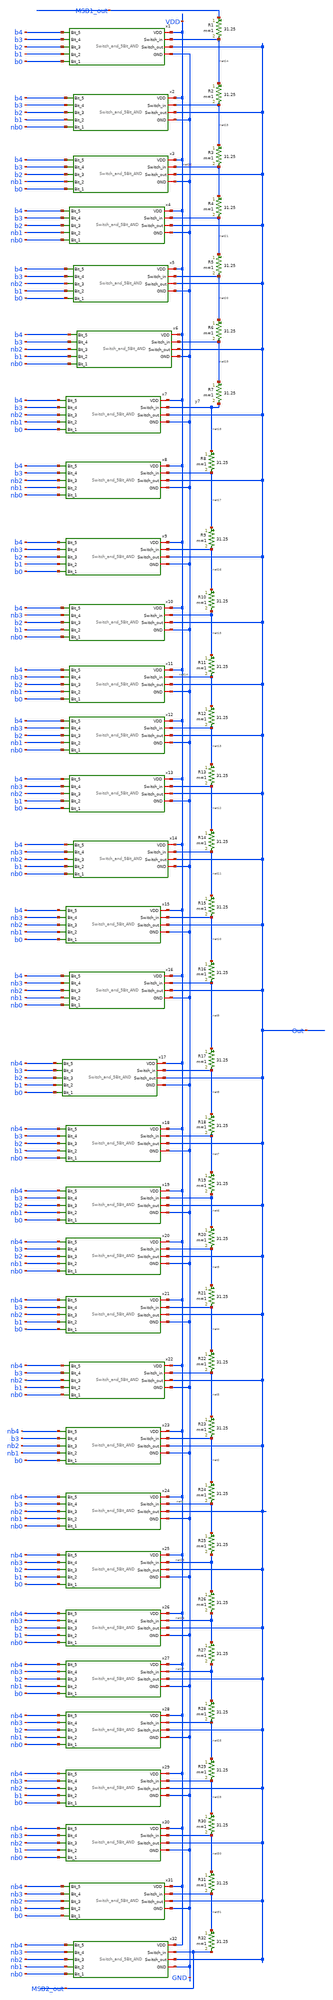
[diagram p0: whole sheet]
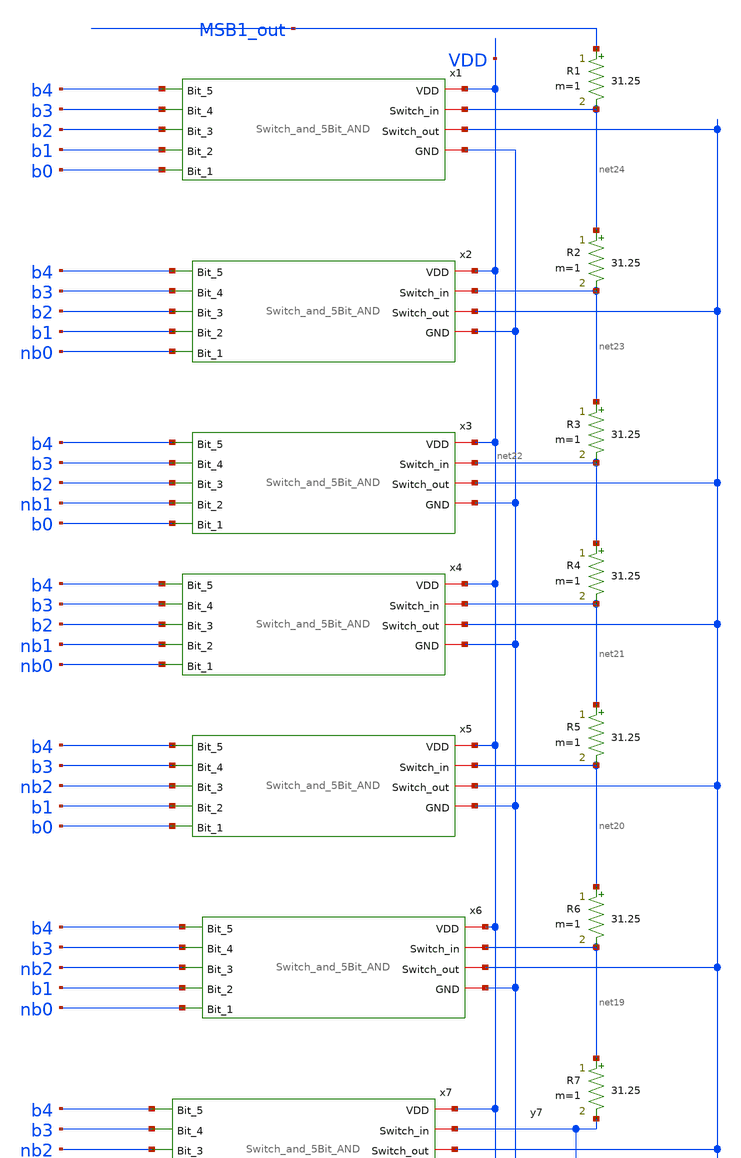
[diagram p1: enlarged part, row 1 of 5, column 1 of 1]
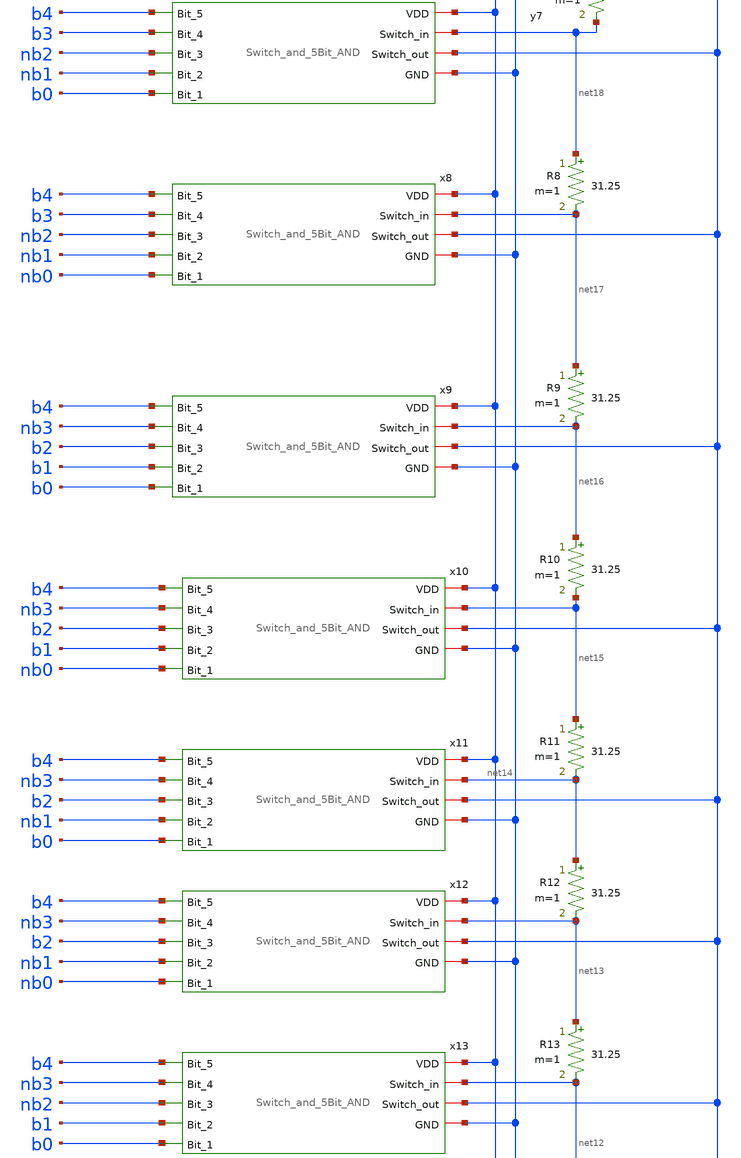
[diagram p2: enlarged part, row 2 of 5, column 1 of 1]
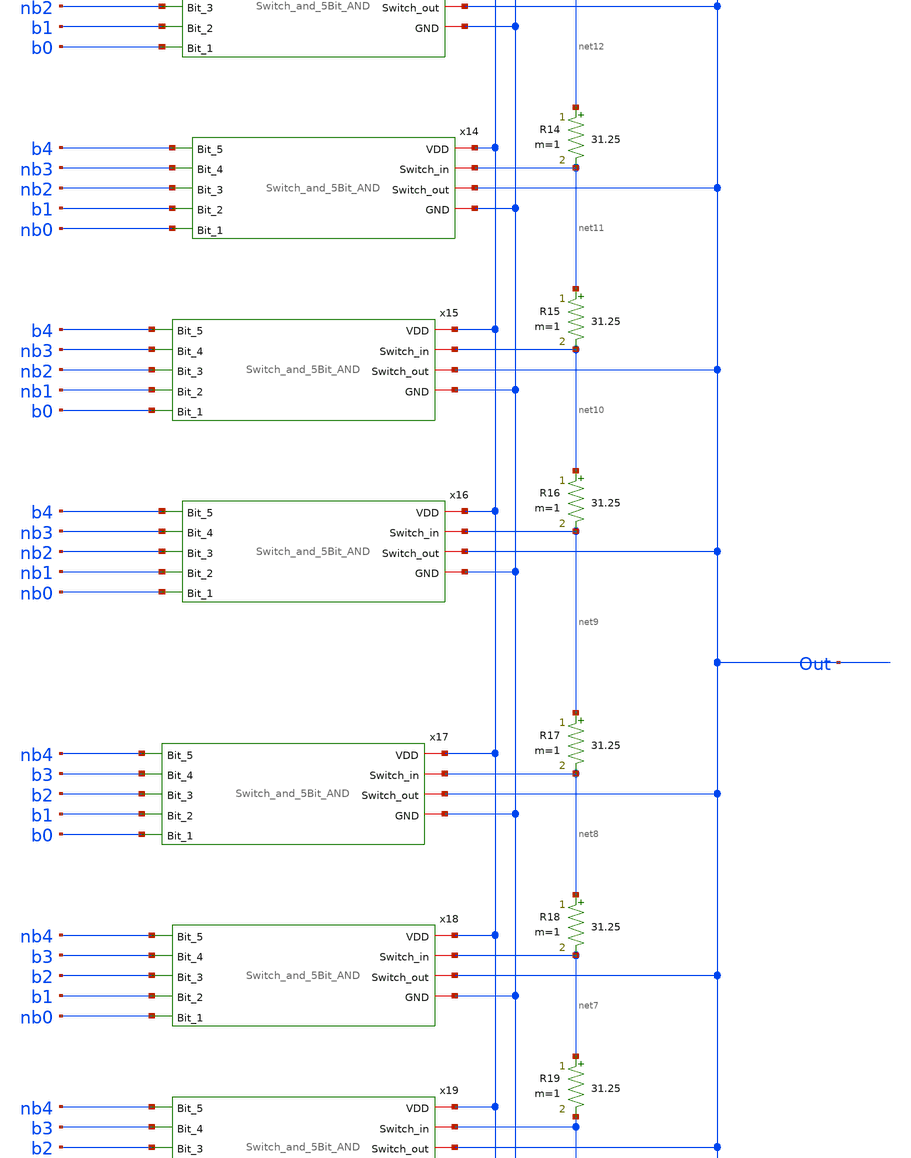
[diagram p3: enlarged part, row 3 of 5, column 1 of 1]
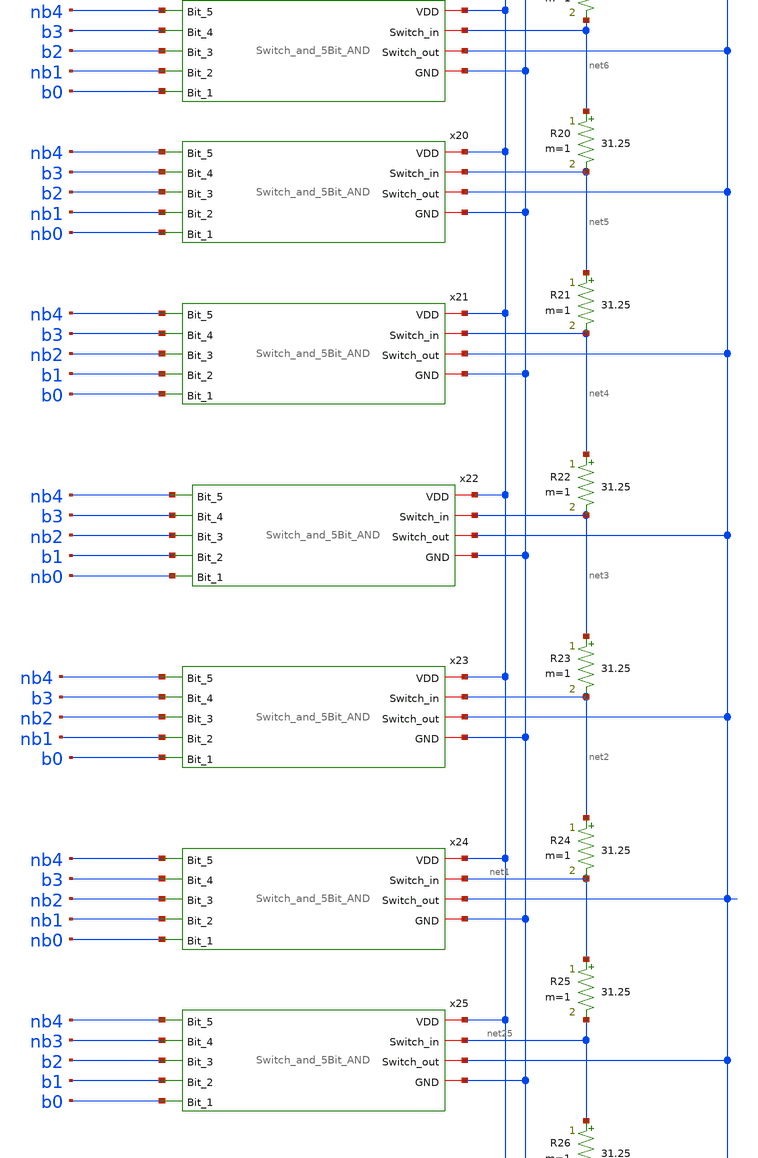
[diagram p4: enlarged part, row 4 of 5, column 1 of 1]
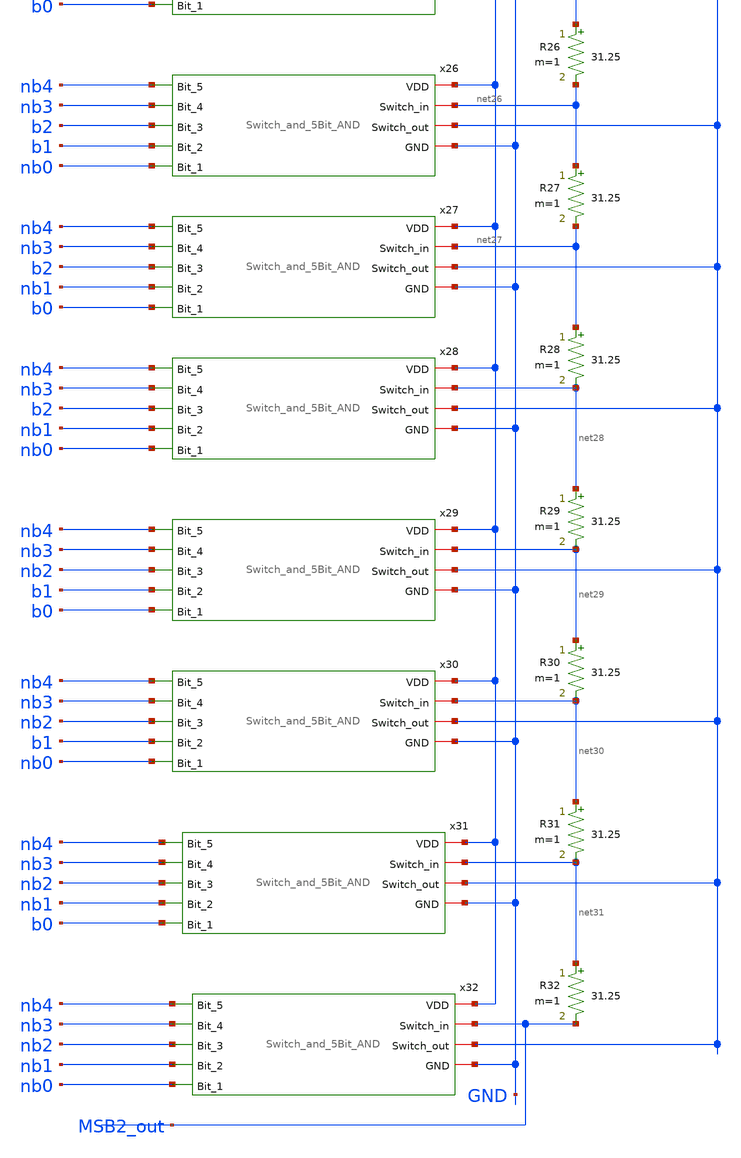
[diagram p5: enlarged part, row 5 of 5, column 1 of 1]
** sch_path: ProjectDesigns/10bitDAC/lsb.sch
**.subckt lsb
R1 MSB1_out net24 31.25 m=1
R2 net24 net23 31.25 m=1
R3 net23 net22 31.25 m=1
R4 net22 net21 31.25 m=1
R5 net21 net20 31.25 m=1
R6 net20 net19 31.25 m=1
R7 net19 net18 31.25 m=1
R8 net18 net17 31.25 m=1
R9 net17 net16 31.25 m=1
R10 net16 net15 31.25 m=1
R11 net15 net14 31.25 m=1
R12 net14 net13 31.25 m=1
R13 net13 net12 31.25 m=1
R14 net12 net11 31.25 m=1
R15 net11 net10 31.25 m=1
R16 net10 net9 31.25 m=1
R17 net9 net8 31.25 m=1
R18 net8 net7 31.25 m=1
R19 net7 net6 31.25 m=1
R20 net6 net5 31.25 m=1
R21 net5 net4 31.25 m=1
R22 net4 net3 31.25 m=1
R23 net3 net2 31.25 m=1
R24 net2 net1 31.25 m=1
R25 net1 net25 31.25 m=1
R26 net25 net26 31.25 m=1
R27 net26 net27 31.25 m=1
R28 net27 net28 31.25 m=1
R29 net28 net29 31.25 m=1
R30 net29 net30 31.25 m=1
R31 net30 net31 31.25 m=1
R32 net31 MSB2_out 31.25 m=1
x1 VDD b4 b3 net24 b2 Out b1 GND b0 Switch_and_5Bit_AND
x2 VDD b4 b3 net23 b2 Out b1 GND nb0 Switch_and_5Bit_AND
x3 VDD b4 b3 net22 b2 Out nb1 GND b0 Switch_and_5Bit_AND
x4 VDD b4 b3 net21 b2 Out nb1 GND nb0 Switch_and_5Bit_AND
x5 VDD b4 b3 net20 nb2 Out b1 GND b0 Switch_and_5Bit_AND
x6 VDD b4 b3 net19 nb2 Out b1 GND nb0 Switch_and_5Bit_AND
x7 VDD b4 b3 net18 nb2 Out nb1 GND b0 Switch_and_5Bit_AND
x8 VDD b4 b3 net17 nb2 Out nb1 GND nb0 Switch_and_5Bit_AND
x9 VDD b4 nb3 net16 b2 Out b1 GND b0 Switch_and_5Bit_AND
x10 VDD b4 nb3 net15 b2 Out b1 GND nb0 Switch_and_5Bit_AND
x11 VDD b4 nb3 net14 b2 Out nb1 GND b0 Switch_and_5Bit_AND
x12 VDD b4 nb3 net13 b2 Out nb1 GND nb0 Switch_and_5Bit_AND
x13 VDD b4 nb3 net12 nb2 Out b1 GND b0 Switch_and_5Bit_AND
x14 VDD b4 nb3 net11 nb2 Out b1 GND nb0 Switch_and_5Bit_AND
x15 VDD b4 nb3 net10 nb2 Out nb1 GND b0 Switch_and_5Bit_AND
x16 VDD b4 nb3 net9 nb2 Out nb1 GND nb0 Switch_and_5Bit_AND
x17 VDD nb4 b3 net8 b2 Out b1 GND b0 Switch_and_5Bit_AND
x18 VDD nb4 b3 net7 b2 Out b1 GND nb0 Switch_and_5Bit_AND
x19 VDD nb4 b3 net6 b2 Out nb1 GND b0 Switch_and_5Bit_AND
x20 VDD nb4 b3 net5 b2 Out nb1 GND nb0 Switch_and_5Bit_AND
x21 VDD nb4 b3 net4 nb2 Out b1 GND b0 Switch_and_5Bit_AND
x22 VDD nb4 b3 net3 nb2 Out b1 GND nb0 Switch_and_5Bit_AND
x23 VDD nb4 b3 net2 nb2 Out nb1 GND b0 Switch_and_5Bit_AND
x24 VDD nb4 b3 net1 nb2 Out nb1 GND nb0 Switch_and_5Bit_AND
x25 VDD nb4 nb3 net25 b2 Out b1 GND b0 Switch_and_5Bit_AND
x26 VDD nb4 nb3 net26 b2 Out b1 GND nb0 Switch_and_5Bit_AND
x27 VDD nb4 nb3 net27 b2 Out nb1 GND b0 Switch_and_5Bit_AND
x28 VDD nb4 nb3 net28 b2 Out nb1 GND nb0 Switch_and_5Bit_AND
x29 VDD nb4 nb3 net29 nb2 Out b1 GND b0 Switch_and_5Bit_AND
x30 VDD nb4 nb3 net30 nb2 Out b1 GND nb0 Switch_and_5Bit_AND
x31 VDD nb4 nb3 net31 nb2 Out nb1 GND b0 Switch_and_5Bit_AND
x32 VDD nb4 nb3 MSB2_out nb2 Out nb1 GND nb0 Switch_and_5Bit_AND
**.ends

* expanding   symbol:  /home/shalini1234/Project/Switch_and_5Bit_AND.sym # of pins=9
** sym_path: ProjectDesigns/Switch_and_5BITAND/Switch_and_5Bit_AND.sym
** sch_path: ProjectDesigns/Switch_and_5BITAND/Switch_and_5Bit_AND.sch
.subckt Switch_and_5Bit_AND VDD Bit_5 Bit_4 Switch_in Bit_3 Switch_out Bit_2 GND Bit_1
*.ipin Bit_5
*.ipin Bit_4
*.ipin Bit_3
*.ipin Bit_2
*.ipin Bit_1
*.iopin Switch_in
*.iopin Switch_out
*.iopin GND
*.iopin VDD
x2 VDD net1 Bit_5 Bit_4 net2 Bit_3 Bit_2 Bit_1 GND 5bit_AND
x1 net1 net2 Switch_in Switch_out GND Switch
.ends


* expanding   symbol:  /home/shalini1234/Project/5bit_AND.sym # of pins=9
** sym_path: ProjectDesigns/5BitAND/5bit_AND.sym
** sch_path: ProjectDesigns/5BitAND/5bit_AND.sch
.subckt 5bit_AND VDD inv_CS_out Bit_5 Bit_4 CS_out Bit_3 Bit_2 Bit_1 GND
*.ipin Bit_1
*.ipin Bit_3
*.ipin Bit_2
*.ipin Bit_4
*.ipin Bit_5
*.iopin inv_CS_out
*.iopin CS_out
*.iopin VDD
*.iopin GND
XM1 inv_CS_out Bit_5 net1 net1 sky130_fd_pr__nfet_01v8 L=0.15 W=1 nf=1 ad='int((nf+1)/2) * W/nf * 0.29'
+ as='int((nf+2)/2) * W/nf * 0.29' pd='2*int((nf+1)/2) * (W/nf + 0.29)' ps='2*int((nf+2)/2) * (W/nf + 0.29)'
+ nrd='0.29 / W' nrs='0.29 / W' sa=0 sb=0 sd=0 mult=1 m=1
XM2 net1 Bit_4 net2 net2 sky130_fd_pr__nfet_01v8 L=0.15 W=1 nf=1 ad='int((nf+1)/2) * W/nf * 0.29' as='int((nf+2)/2) * W/nf * 0.29'
+ pd='2*int((nf+1)/2) * (W/nf + 0.29)' ps='2*int((nf+2)/2) * (W/nf + 0.29)' nrd='0.29 / W' nrs='0.29 / W'
+ sa=0 sb=0 sd=0 mult=1 m=1
XM3 net2 Bit_3 net3 net3 sky130_fd_pr__nfet_01v8 L=0.15 W=1 nf=1 ad='int((nf+1)/2) * W/nf * 0.29' as='int((nf+2)/2) * W/nf * 0.29'
+ pd='2*int((nf+1)/2) * (W/nf + 0.29)' ps='2*int((nf+2)/2) * (W/nf + 0.29)' nrd='0.29 / W' nrs='0.29 / W'
+ sa=0 sb=0 sd=0 mult=1 m=1
XM4 net3 Bit_2 net4 net4 sky130_fd_pr__nfet_01v8 L=0.15 W=1 nf=1 ad='int((nf+1)/2) * W/nf * 0.29' as='int((nf+2)/2) * W/nf * 0.29'
+ pd='2*int((nf+1)/2) * (W/nf + 0.29)' ps='2*int((nf+2)/2) * (W/nf + 0.29)' nrd='0.29 / W' nrs='0.29 / W'
+ sa=0 sb=0 sd=0 mult=1 m=1
XM5 net4 Bit_1 GND GND sky130_fd_pr__nfet_01v8 L=0.15 W=1 nf=1 ad='int((nf+1)/2) * W/nf * 0.29' as='int((nf+2)/2) * W/nf * 0.29'
+ pd='2*int((nf+1)/2) * (W/nf + 0.29)' ps='2*int((nf+2)/2) * (W/nf + 0.29)' nrd='0.29 / W' nrs='0.29 / W'
+ sa=0 sb=0 sd=0 mult=1 m=1
XM6 inv_CS_out Bit_3 VDD VDD sky130_fd_pr__pfet_01v8 L=0.15 W=1 nf=1 ad='int((nf+1)/2) * W/nf * 0.29'
+ as='int((nf+2)/2) * W/nf * 0.29' pd='2*int((nf+1)/2) * (W/nf + 0.29)' ps='2*int((nf+2)/2) * (W/nf + 0.29)'
+ nrd='0.29 / W' nrs='0.29 / W' sa=0 sb=0 sd=0 mult=1 m=1
XM7 inv_CS_out Bit_2 VDD VDD sky130_fd_pr__pfet_01v8 L=0.15 W=1 nf=1 ad='int((nf+1)/2) * W/nf * 0.29'
+ as='int((nf+2)/2) * W/nf * 0.29' pd='2*int((nf+1)/2) * (W/nf + 0.29)' ps='2*int((nf+2)/2) * (W/nf + 0.29)'
+ nrd='0.29 / W' nrs='0.29 / W' sa=0 sb=0 sd=0 mult=1 m=1
XM8 inv_CS_out Bit_1 VDD VDD sky130_fd_pr__pfet_01v8 L=0.15 W=1 nf=1 ad='int((nf+1)/2) * W/nf * 0.29'
+ as='int((nf+2)/2) * W/nf * 0.29' pd='2*int((nf+1)/2) * (W/nf + 0.29)' ps='2*int((nf+2)/2) * (W/nf + 0.29)'
+ nrd='0.29 / W' nrs='0.29 / W' sa=0 sb=0 sd=0 mult=1 m=1
XM9 inv_CS_out Bit_4 VDD VDD sky130_fd_pr__pfet_01v8 L=0.15 W=1 nf=1 ad='int((nf+1)/2) * W/nf * 0.29'
+ as='int((nf+2)/2) * W/nf * 0.29' pd='2*int((nf+1)/2) * (W/nf + 0.29)' ps='2*int((nf+2)/2) * (W/nf + 0.29)'
+ nrd='0.29 / W' nrs='0.29 / W' sa=0 sb=0 sd=0 mult=1 m=1
XM10 inv_CS_out Bit_5 VDD VDD sky130_fd_pr__pfet_01v8 L=0.15 W=1 nf=1 ad='int((nf+1)/2) * W/nf * 0.29'
+ as='int((nf+2)/2) * W/nf * 0.29' pd='2*int((nf+1)/2) * (W/nf + 0.29)' ps='2*int((nf+2)/2) * (W/nf + 0.29)'
+ nrd='0.29 / W' nrs='0.29 / W' sa=0 sb=0 sd=0 mult=1 m=1
XM11 CS_out inv_CS_out GND GND sky130_fd_pr__nfet_01v8 L=0.15 W=1 nf=1 ad='int((nf+1)/2) * W/nf * 0.29'
+ as='int((nf+2)/2) * W/nf * 0.29' pd='2*int((nf+1)/2) * (W/nf + 0.29)' ps='2*int((nf+2)/2) * (W/nf + 0.29)'
+ nrd='0.29 / W' nrs='0.29 / W' sa=0 sb=0 sd=0 mult=1 m=1
XM12 CS_out inv_CS_out VDD VDD sky130_fd_pr__pfet_01v8 L=0.15 W=1 nf=1 ad='int((nf+1)/2) * W/nf * 0.29'
+ as='int((nf+2)/2) * W/nf * 0.29' pd='2*int((nf+1)/2) * (W/nf + 0.29)' ps='2*int((nf+2)/2) * (W/nf + 0.29)'
+ nrd='0.29 / W' nrs='0.29 / W' sa=0 sb=0 sd=0 mult=1 m=1
.ends


* expanding   symbol:  /home/shalini1234/Project/Switch.sym # of pins=5
** sym_path: ProjectDesigns/Switch/Switch.sym
** sch_path: ProjectDesigns/Switch/Switch.sch
.subckt Switch inv_CS CS Switch_in Switch_out GND
*.iopin Switch_in
*.iopin Switch_out
*.iopin CS
*.iopin inv_CS
*.iopin GND
XM1 Switch_in CS Switch_out Switch_out sky130_fd_pr__nfet_01v8 L=0.15 W=1 nf=1 ad='int((nf+1)/2) * W/nf * 0.29'
+ as='int((nf+2)/2) * W/nf * 0.29' pd='2*int((nf+1)/2) * (W/nf + 0.29)' ps='2*int((nf+2)/2) * (W/nf + 0.29)'
+ nrd='0.29 / W' nrs='0.29 / W' sa=0 sb=0 sd=0 mult=1 m=1
XM2 Switch_out inv_CS Switch_in Switch_in sky130_fd_pr__pfet_01v8 L=0.15 W=1 nf=1 ad='int((nf+1)/2) * W/nf * 0.29'
+ as='int((nf+2)/2) * W/nf * 0.29' pd='2*int((nf+1)/2) * (W/nf + 0.29)' ps='2*int((nf+2)/2) * (W/nf + 0.29)'
+ nrd='0.29 / W' nrs='0.29 / W' sa=0 sb=0 sd=0 mult=1 m=1
XM5 Switch_out inv_CS GND GND sky130_fd_pr__nfet_01v8 L=0.15 W=1 nf=1 ad='int((nf+1)/2) * W/nf * 0.29'
+ as='int((nf+2)/2) * W/nf * 0.29' pd='2*int((nf+1)/2) * (W/nf + 0.29)' ps='2*int((nf+2)/2) * (W/nf + 0.29)'
+ nrd='0.29 / W' nrs='0.29 / W' sa=0 sb=0 sd=0 mult=1 m=1
.ends

.end
